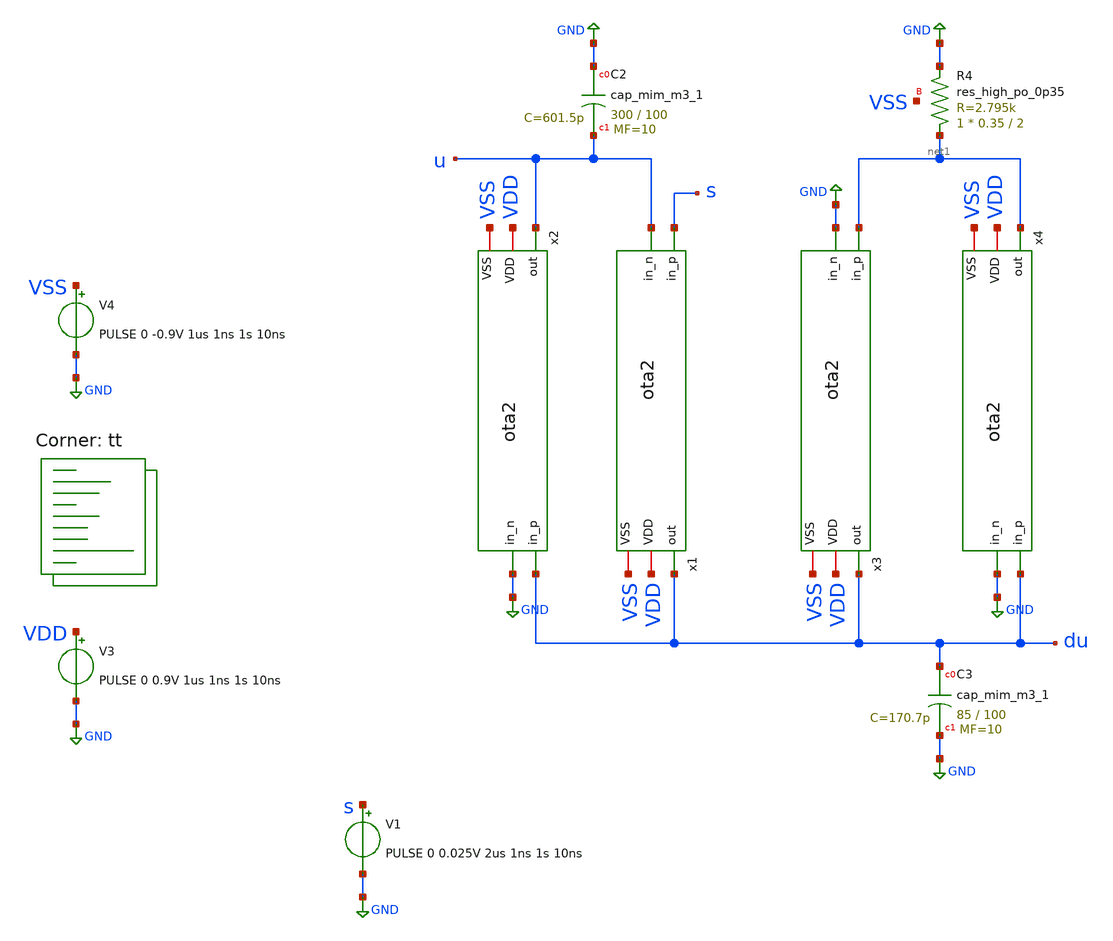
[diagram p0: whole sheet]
** sch_path: xschem/tests/oscilator/unstable_oscilator_test.sch
**.subckt unstable_oscilator_test
V3 VDD GND PULSE 0 0.9V 1us 1ns 1s 10ns
V4 VSS GND PULSE 0 -0.9V 1us 1ns 1s 10ns
V1 s GND PULSE 0 0.025V 2us 1ns 1s 10ns
x2 u du GND VDD VSS ota2
x1 du s u VDD VSS ota2
x3 du net1 GND VDD VSS ota2
x4 net1 du GND VDD VSS ota2
XR4 net1 GND VSS sky130_fd_pr__res_high_po_0p35 L=2 mult=1 m=1
XC2 GND u sky130_fd_pr__cap_mim_m3_1 W=300 L=100 MF=10 m=10
XC3 du GND sky130_fd_pr__cap_mim_m3_1 W=85 L=100 MF=10 m=10
**** begin user architecture code
 *.lib $::SKYWATER_MODELS/sky130.lib.spice tt
.include $::SKYWATER_STDCELLS/sky130_fd_sc_hd.spice



* Here's a comment
.options acct list
.options method=gear
.temp 25
*vvcc VDD 0 dc 1.8
*vvss VSS 0 0
.control
save all
ic v(u)=0.01 v(s)=0.3
tran 0.001u 50u uic
plot u du s
write unstable_oscilator_test.raw
.endc


.lib $::SKYWATER_MODELS/sky130.lib.spice tt
**** end user architecture code
**.ends
.GLOBAL GND
.end
